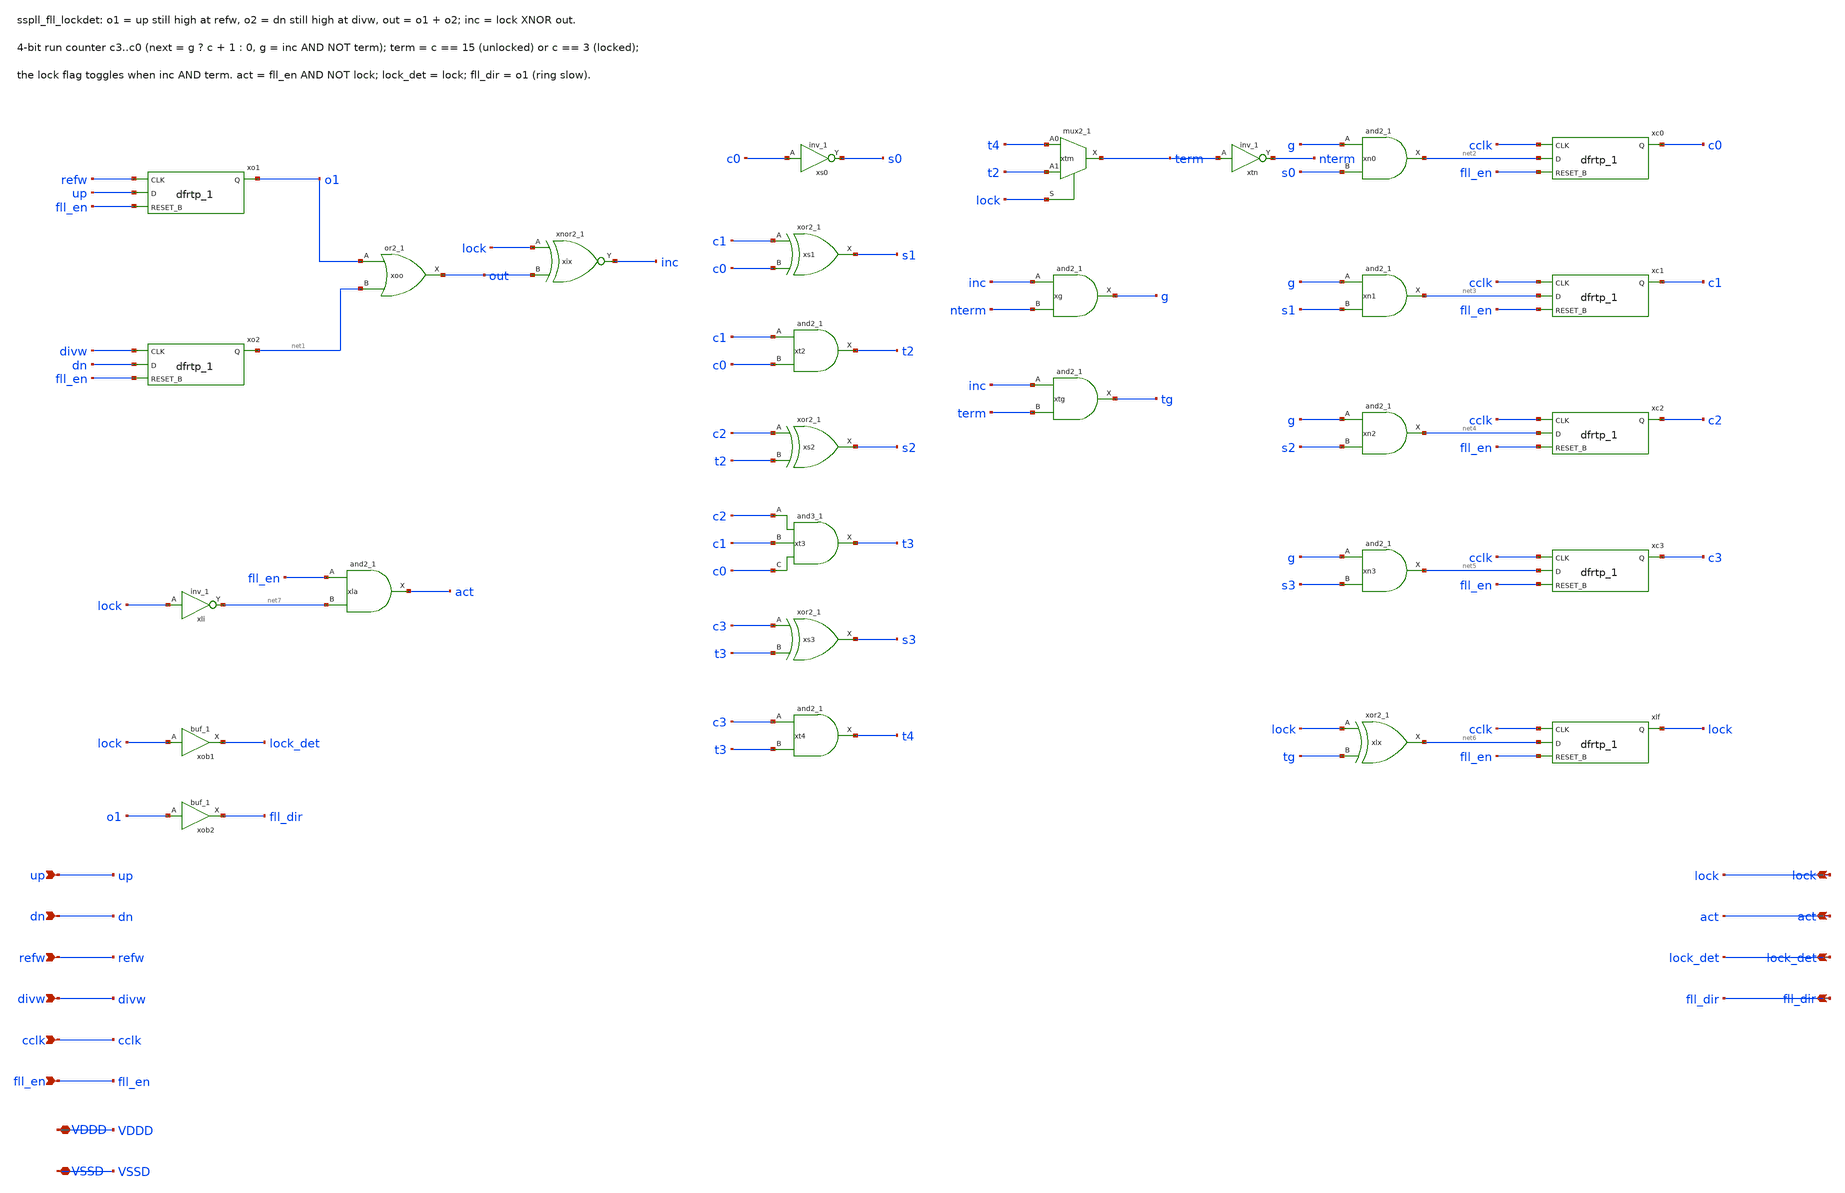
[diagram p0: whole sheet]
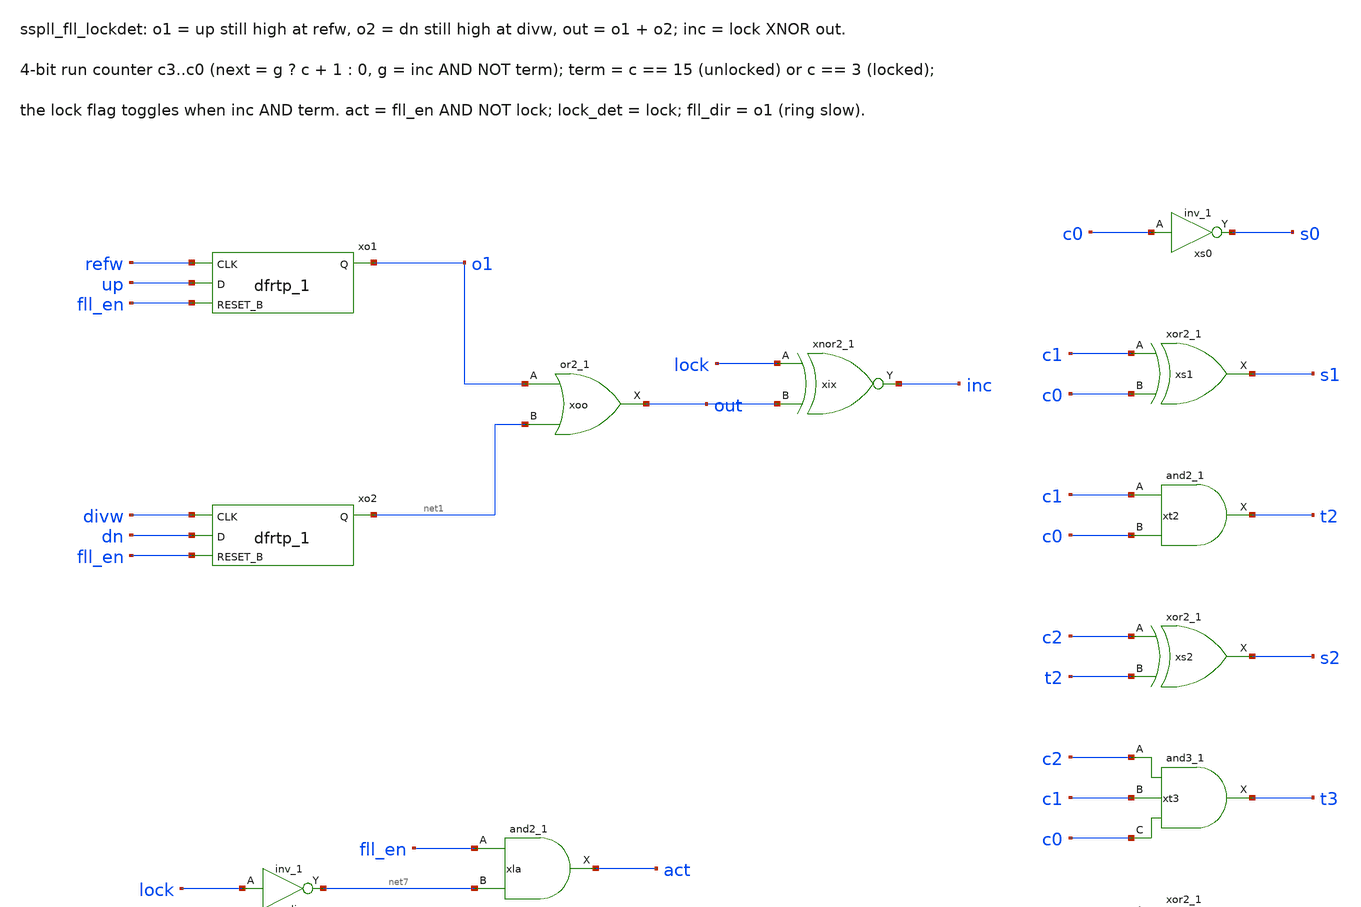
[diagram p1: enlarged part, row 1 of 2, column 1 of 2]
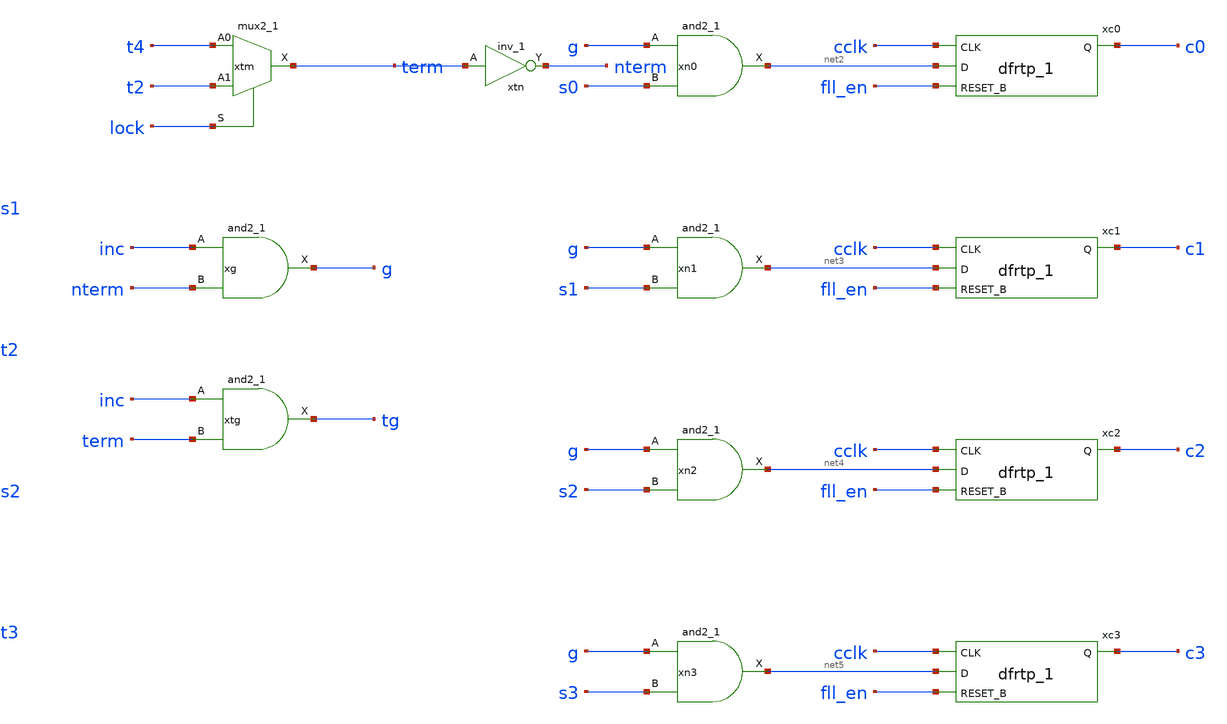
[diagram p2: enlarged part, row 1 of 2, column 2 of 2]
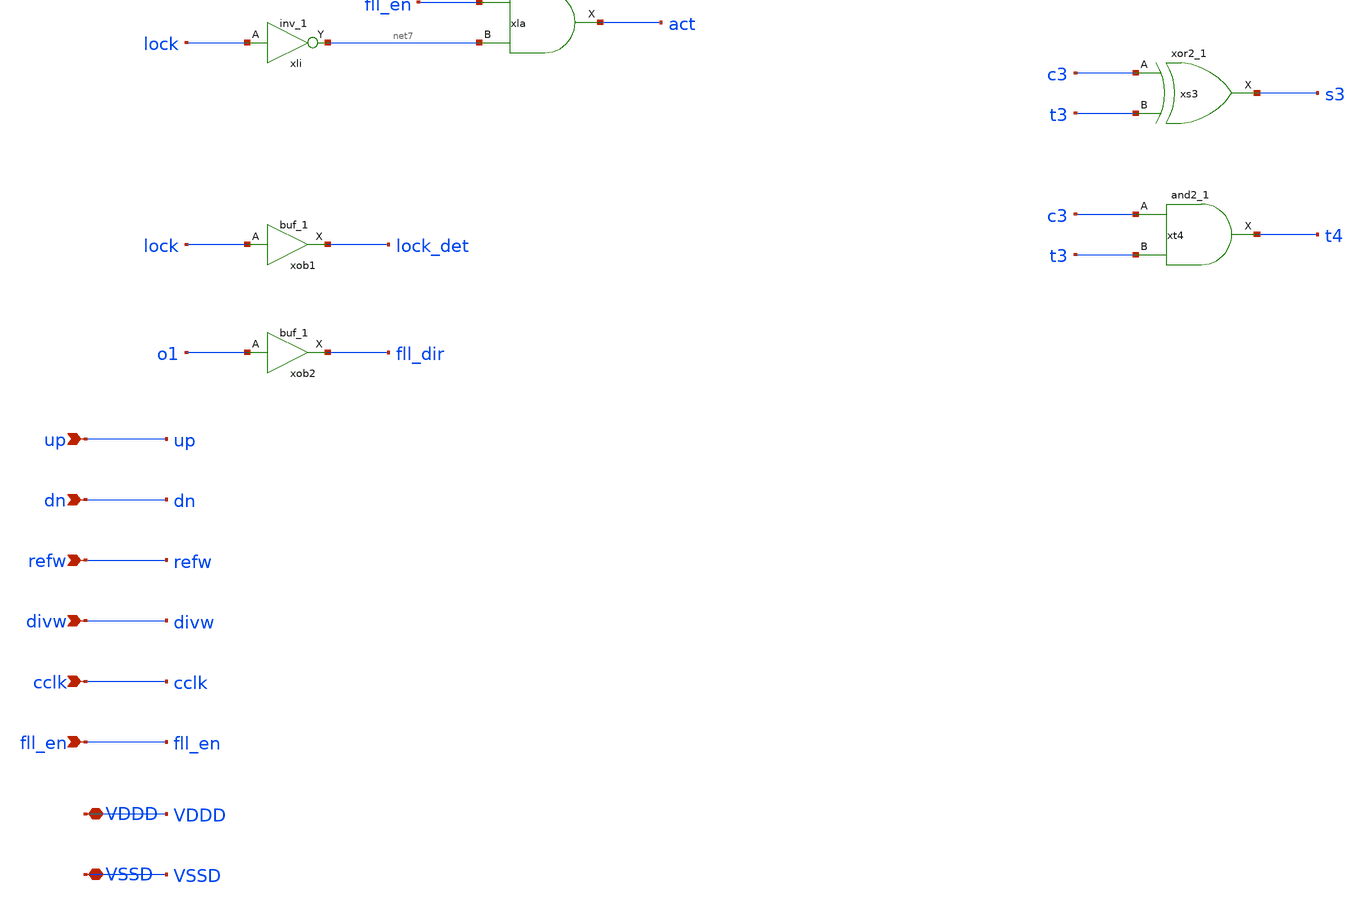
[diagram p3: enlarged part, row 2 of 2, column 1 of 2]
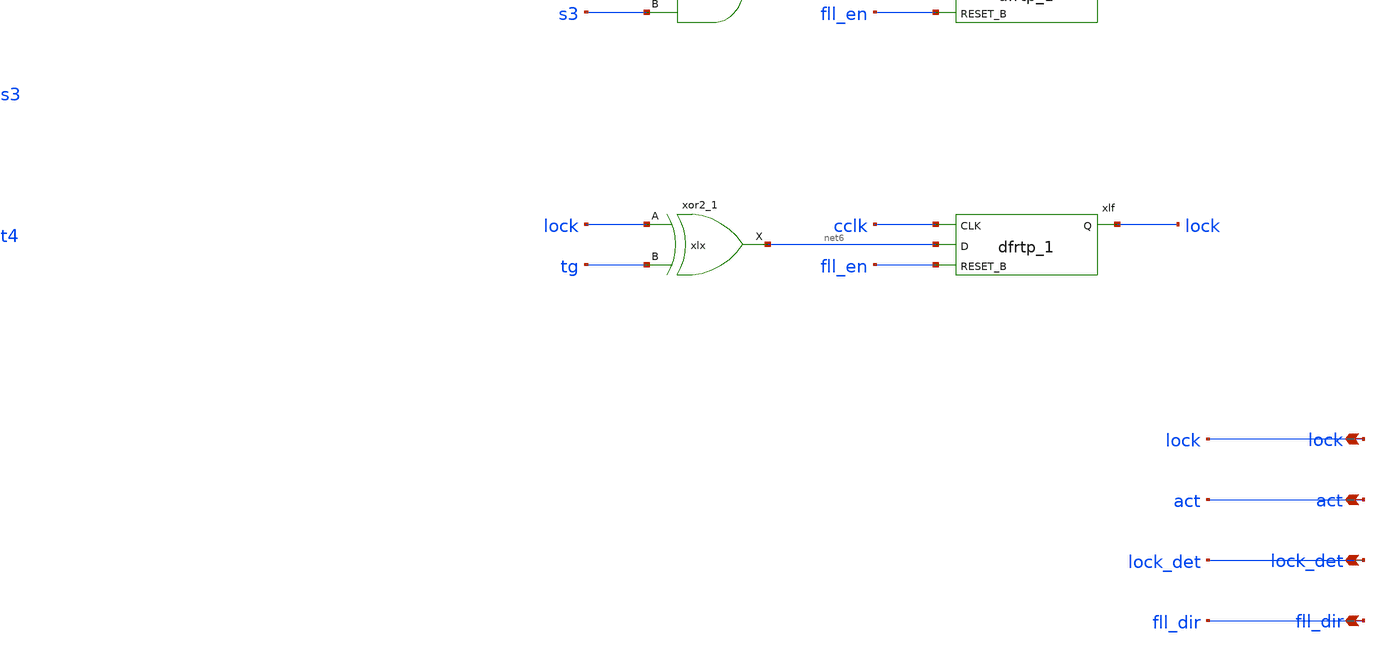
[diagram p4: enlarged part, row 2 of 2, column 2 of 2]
** sch_path: xschem/fll_hv/sspll_fll_lockdet.sch
**.subckt sspll_fll_lockdet up dn refw divw cclk fll_en lock act lock_det fll_dir VDDD VSSD
*.ipin up
*.ipin dn
*.ipin refw
*.ipin divw
*.ipin cclk
*.ipin fll_en
*.opin lock
*.opin act
*.opin lock_det
*.opin fll_dir
*.iopin VDDD
*.iopin VSSD
xo1 refw up fll_en VSSD VSSD VDDD VDDD o1 sky130_fd_sc_hd__dfrtp_1
xo2 divw dn fll_en VSSD VSSD VDDD VDDD net1 sky130_fd_sc_hd__dfrtp_1
xoo o1 net1 VSSD VSSD VDDD VDDD out sky130_fd_sc_hd__or2_1
xix lock out VSSD VSSD VDDD VDDD inc sky130_fd_sc_hd__xnor2_1
xs0 c0 VSSD VSSD VDDD VDDD s0 sky130_fd_sc_hd__inv_1
xs1 c1 c0 VSSD VSSD VDDD VDDD s1 sky130_fd_sc_hd__xor2_1
xt2 c1 c0 VSSD VSSD VDDD VDDD t2 sky130_fd_sc_hd__and2_1
xs2 c2 t2 VSSD VSSD VDDD VDDD s2 sky130_fd_sc_hd__xor2_1
xt3 c2 c1 c0 VSSD VSSD VDDD VDDD t3 sky130_fd_sc_hd__and3_1
xs3 c3 t3 VSSD VSSD VDDD VDDD s3 sky130_fd_sc_hd__xor2_1
xt4 c3 t3 VSSD VSSD VDDD VDDD t4 sky130_fd_sc_hd__and2_1
xtm t4 t2 lock VSSD VSSD VDDD VDDD term sky130_fd_sc_hd__mux2_1
xtn term VSSD VSSD VDDD VDDD nterm sky130_fd_sc_hd__inv_1
xg inc nterm VSSD VSSD VDDD VDDD g sky130_fd_sc_hd__and2_1
xtg inc term VSSD VSSD VDDD VDDD tg sky130_fd_sc_hd__and2_1
xn0 g s0 VSSD VSSD VDDD VDDD net2 sky130_fd_sc_hd__and2_1
xc0 cclk net2 fll_en VSSD VSSD VDDD VDDD c0 sky130_fd_sc_hd__dfrtp_1
xn1 g s1 VSSD VSSD VDDD VDDD net3 sky130_fd_sc_hd__and2_1
xc1 cclk net3 fll_en VSSD VSSD VDDD VDDD c1 sky130_fd_sc_hd__dfrtp_1
xn2 g s2 VSSD VSSD VDDD VDDD net4 sky130_fd_sc_hd__and2_1
xc2 cclk net4 fll_en VSSD VSSD VDDD VDDD c2 sky130_fd_sc_hd__dfrtp_1
xn3 g s3 VSSD VSSD VDDD VDDD net5 sky130_fd_sc_hd__and2_1
xc3 cclk net5 fll_en VSSD VSSD VDDD VDDD c3 sky130_fd_sc_hd__dfrtp_1
xlx lock tg VSSD VSSD VDDD VDDD net6 sky130_fd_sc_hd__xor2_1
xlf cclk net6 fll_en VSSD VSSD VDDD VDDD lock sky130_fd_sc_hd__dfrtp_1
xli lock VSSD VSSD VDDD VDDD net7 sky130_fd_sc_hd__inv_1
xla fll_en net7 VSSD VSSD VDDD VDDD act sky130_fd_sc_hd__and2_1
xob1 lock VSSD VSSD VDDD VDDD lock_det sky130_fd_sc_hd__buf_1
xob2 o1 VSSD VSSD VDDD VDDD fll_dir sky130_fd_sc_hd__buf_1
**.ends
.end
